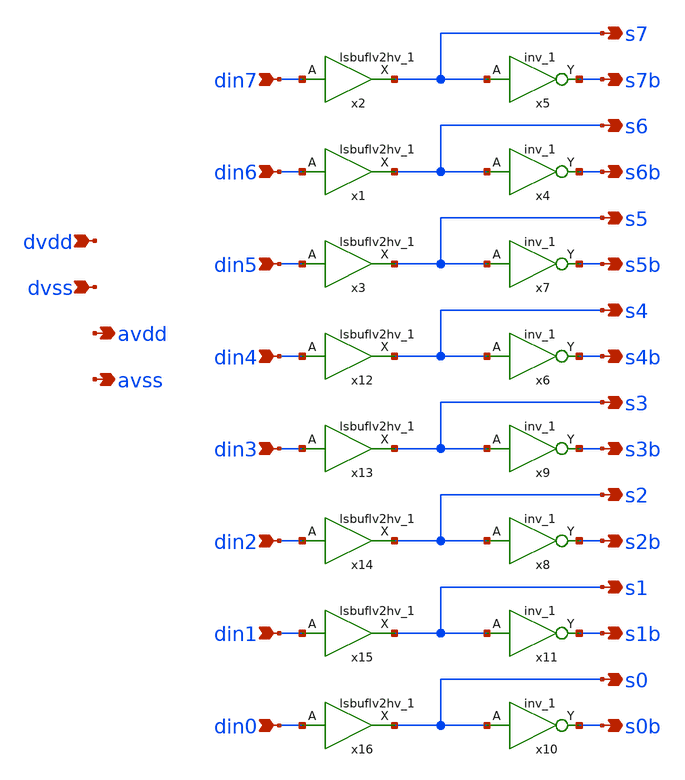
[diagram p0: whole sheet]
** sch_path: xschem/dvdd_to_avdd.sch
**.subckt dvdd_to_avdd din0 din1 din2 din3 din4 din5 din6 din7 s7 s7b s6 s6b s5 s5b s4 s4b s3 s3b s2
*+ s2b s1 s1b s0 s0b dvdd avdd dvss avss
*.ipin din0
*.ipin din1
*.ipin din2
*.ipin din3
*.ipin din4
*.ipin din5
*.ipin din6
*.ipin din7
*.opin s7
*.opin s7b
*.opin s6
*.opin s6b
*.opin s5
*.opin s5b
*.opin s4
*.opin s4b
*.opin s3
*.opin s3b
*.opin s2
*.opin s2b
*.opin s1
*.opin s1b
*.opin s0
*.opin s0b
*.ipin dvdd
*.opin avdd
*.ipin dvss
*.opin avss
x4 s6 avss avss avdd avdd s6b sky130_fd_sc_hvl__inv_1
x5 s7 avss avss avdd avdd s7b sky130_fd_sc_hvl__inv_1
x6 s4 avss avss avdd avdd s4b sky130_fd_sc_hvl__inv_1
x7 s5 avss avss avdd avdd s5b sky130_fd_sc_hvl__inv_1
x8 s2 avss avss avdd avdd s2b sky130_fd_sc_hvl__inv_1
x9 s3 avss avss avdd avdd s3b sky130_fd_sc_hvl__inv_1
x10 s0 avss avss avdd avdd s0b sky130_fd_sc_hvl__inv_1
x11 s1 avss avss avdd avdd s1b sky130_fd_sc_hvl__inv_1
x2 din7 dvdd dvss dvss avdd avdd s7 sky130_fd_sc_hvl__lsbuflv2hv_1
x1 din6 dvdd dvss dvss avdd avdd s6 sky130_fd_sc_hvl__lsbuflv2hv_1
x3 din5 dvdd dvss dvss avdd avdd s5 sky130_fd_sc_hvl__lsbuflv2hv_1
x12 din4 dvdd dvss dvss avdd avdd s4 sky130_fd_sc_hvl__lsbuflv2hv_1
x13 din3 dvdd dvss dvss avdd avdd s3 sky130_fd_sc_hvl__lsbuflv2hv_1
x14 din2 dvdd dvss dvss avdd avdd s2 sky130_fd_sc_hvl__lsbuflv2hv_1
x15 din1 dvdd dvss dvss avdd avdd s1 sky130_fd_sc_hvl__lsbuflv2hv_1
x16 din0 dvdd dvss dvss avdd avdd s0 sky130_fd_sc_hvl__lsbuflv2hv_1
**.ends
.end
